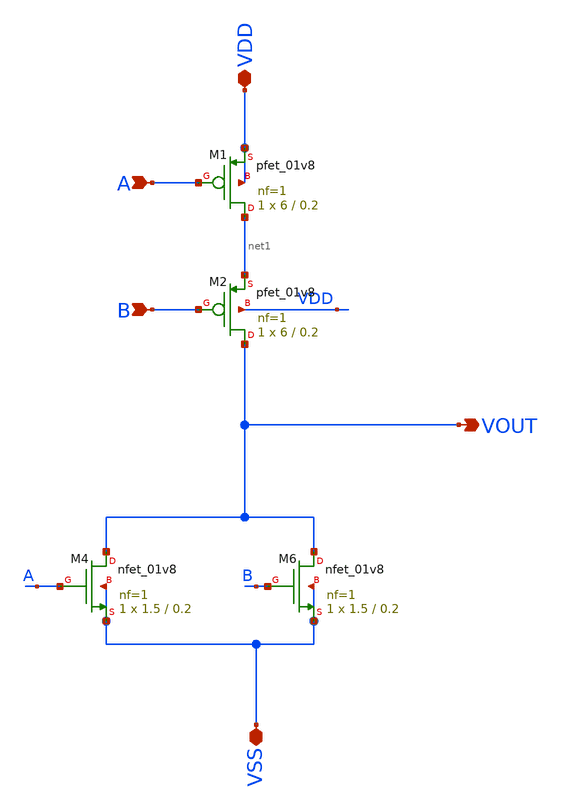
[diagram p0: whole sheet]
** sch_path: Xschem/PLL_TOP_Schematics/NOR_1.sch
**.subckt NOR_1 VSS VDD A B VOUT
*.iopin VSS
*.iopin VDD
*.ipin A
*.ipin B
*.opin VOUT
XM1 net1 A VDD VDD sky130_fd_pr__pfet_01v8 L=0.2 W=6 nf=1 ad='int((nf+1)/2) * W/nf * 0.29' as='int((nf+2)/2) * W/nf * 0.29'
+ pd='2*int((nf+1)/2) * (W/nf + 0.29)' ps='2*int((nf+2)/2) * (W/nf + 0.29)' nrd='0.29 / W' nrs='0.29 / W'
+ sa=0 sb=0 sd=0 mult=1 m=1
XM2 VOUT B net1 VDD sky130_fd_pr__pfet_01v8 L=0.2 W=6 nf=1 ad='int((nf+1)/2) * W/nf * 0.29' as='int((nf+2)/2) * W/nf * 0.29'
+ pd='2*int((nf+1)/2) * (W/nf + 0.29)' ps='2*int((nf+2)/2) * (W/nf + 0.29)' nrd='0.29 / W' nrs='0.29 / W'
+ sa=0 sb=0 sd=0 mult=1 m=1
XM4 VOUT A VSS VSS sky130_fd_pr__nfet_01v8 L=0.2 W=1.5 nf=1 ad='int((nf+1)/2) * W/nf * 0.29' as='int((nf+2)/2) * W/nf * 0.29'
+ pd='2*int((nf+1)/2) * (W/nf + 0.29)' ps='2*int((nf+2)/2) * (W/nf + 0.29)' nrd='0.29 / W' nrs='0.29 / W'
+ sa=0 sb=0 sd=0 mult=1 m=1
XM6 VOUT B VSS VSS sky130_fd_pr__nfet_01v8 L=0.2 W=1.5 nf=1 ad='int((nf+1)/2) * W/nf * 0.29' as='int((nf+2)/2) * W/nf * 0.29'
+ pd='2*int((nf+1)/2) * (W/nf + 0.29)' ps='2*int((nf+2)/2) * (W/nf + 0.29)' nrd='0.29 / W' nrs='0.29 / W'
+ sa=0 sb=0 sd=0 mult=1 m=1
**.ends
.end
